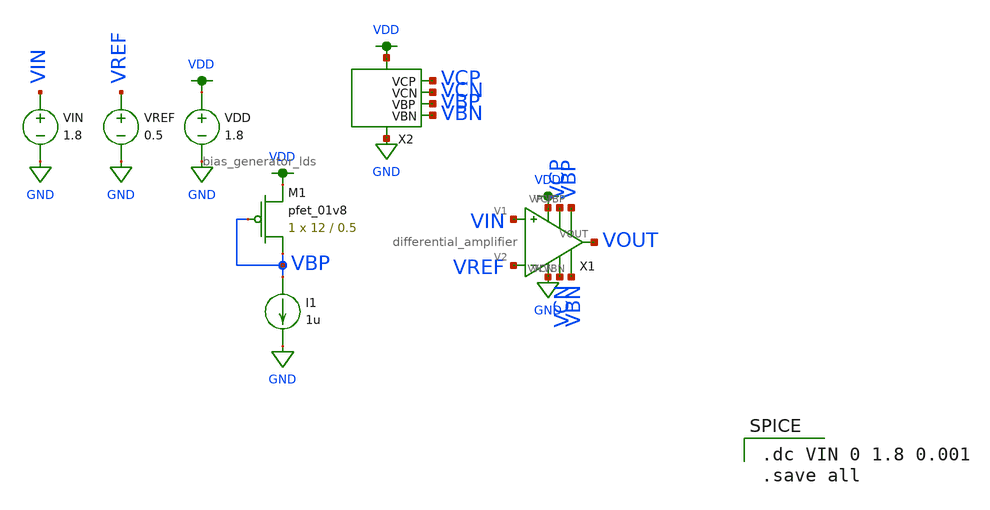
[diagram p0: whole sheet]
** sch_path: mp3/schematics/bias_generator_tran.sch
**.subckt bias_generator_tran
VDD VDD GND 1.8
I1 VBP GND 1u
VREF VREF GND 0.5
VIN VIN GND 1.8
XM1 VBP VBP VDD VDD sky130_fd_pr__pfet_01v8 L=0.5 W=12 nf=1 ad='int((nf+1)/2) * W/nf * 0.29' as='int((nf+2)/2) * W/nf * 0.29'
+ pd='2*int((nf+1)/2) * (W/nf + 0.29)' ps='2*int((nf+2)/2) * (W/nf + 0.29)' nrd='0.29 / W' nrs='0.29 / W'
+ sa=0 sb=0 sd=0 mult=1 m=1
X1 VIN VREF VDD GND VCN VBN VBP VCP VOUT differential_amplifier
X2 VDD GND VCN VCP VBP VBN bias_generator_lds
**** begin user architecture code

.option wnflag=1
.lib ~/skywater/skywater-pdk/libraries/sky130_fd_pr_ngspice/latest/models/sky130.lib.spice tt


.dc VIN 0 1.8 0.001
.save all

**** end user architecture code
**.ends

* expanding   symbol:  /home/madvlsi/Documents/VLSI/mp3/schematics/differential_amplifier.sym # of
*+ pins=9
** sym_path: mp3/schematics/differential_amplifier.sym
** sch_path: mp3/schematics/differential_amplifier.sch
.subckt differential_amplifier V1 V2 VP VN VCN VBN VBP VCP VOUT
*.iopin VBP
*.iopin VCP
*.ipin V1
*.ipin V2
*.iopin VBN
*.iopin VCN
*.iopin VP
*.iopin VN
*.opin VOUT
XM3b VP VBP net1 VDD sky130_fd_pr__pfet_01v8 L=0.5 W=3 nf=1 ad='int((nf+1)/2) * W/nf * 0.29' as='int((nf+2)/2) * W/nf * 0.29'
+ pd='2*int((nf+1)/2) * (W/nf + 0.29)' ps='2*int((nf+2)/2) * (W/nf + 0.29)' nrd='0.29 / W' nrs='0.29 / W'
+ sa=0 sb=0 sd=0 mult=1 m=1
XM3a net2 VBP VP VDD sky130_fd_pr__pfet_01v8 L=0.5 W=3 nf=1 ad='int((nf+1)/2) * W/nf * 0.29' as='int((nf+2)/2) * W/nf * 0.29'
+ pd='2*int((nf+1)/2) * (W/nf + 0.29)' ps='2*int((nf+2)/2) * (W/nf + 0.29)' nrd='0.29 / W' nrs='0.29 / W'
+ sa=0 sb=0 sd=0 mult=1 m=1
XM4a net1 VBP VP VDD sky130_fd_pr__pfet_01v8 L=0.5 W=3 nf=1 ad='int((nf+1)/2) * W/nf * 0.29' as='int((nf+2)/2) * W/nf * 0.29'
+ pd='2*int((nf+1)/2) * (W/nf + 0.29)' ps='2*int((nf+2)/2) * (W/nf + 0.29)' nrd='0.29 / W' nrs='0.29 / W'
+ sa=0 sb=0 sd=0 mult=1 m=1
XM4b VP VBP net2 VDD sky130_fd_pr__pfet_01v8 L=0.5 W=3 nf=1 ad='int((nf+1)/2) * W/nf * 0.29' as='int((nf+2)/2) * W/nf * 0.29'
+ pd='2*int((nf+1)/2) * (W/nf + 0.29)' ps='2*int((nf+2)/2) * (W/nf + 0.29)' nrd='0.29 / W' nrs='0.29 / W'
+ sa=0 sb=0 sd=0 mult=1 m=1
XM3c net2 VBP VP VDD sky130_fd_pr__pfet_01v8 L=0.5 W=3 nf=1 ad='int((nf+1)/2) * W/nf * 0.29' as='int((nf+2)/2) * W/nf * 0.29'
+ pd='2*int((nf+1)/2) * (W/nf + 0.29)' ps='2*int((nf+2)/2) * (W/nf + 0.29)' nrd='0.29 / W' nrs='0.29 / W'
+ sa=0 sb=0 sd=0 mult=1 m=1
XM3d VP VBP net1 VDD sky130_fd_pr__pfet_01v8 L=0.5 W=3 nf=1 ad='int((nf+1)/2) * W/nf * 0.29' as='int((nf+2)/2) * W/nf * 0.29'
+ pd='2*int((nf+1)/2) * (W/nf + 0.29)' ps='2*int((nf+2)/2) * (W/nf + 0.29)' nrd='0.29 / W' nrs='0.29 / W'
+ sa=0 sb=0 sd=0 mult=1 m=1
XM4c net1 VBP VP VDD sky130_fd_pr__pfet_01v8 L=0.5 W=3 nf=1 ad='int((nf+1)/2) * W/nf * 0.29' as='int((nf+2)/2) * W/nf * 0.29'
+ pd='2*int((nf+1)/2) * (W/nf + 0.29)' ps='2*int((nf+2)/2) * (W/nf + 0.29)' nrd='0.29 / W' nrs='0.29 / W'
+ sa=0 sb=0 sd=0 mult=1 m=1
XM1e VP VP net2 VP sky130_fd_pr__pfet_01v8 L=0.5 W=3 nf=1 ad='int((nf+1)/2) * W/nf * 0.29' as='int((nf+2)/2) * W/nf * 0.29'
+ pd='2*int((nf+1)/2) * (W/nf + 0.29)' ps='2*int((nf+2)/2) * (W/nf + 0.29)' nrd='0.29 / W' nrs='0.29 / W'
+ sa=0 sb=0 sd=0 mult=1 m=1
XM1f net2 VP VP VP sky130_fd_pr__pfet_01v8 L=0.5 W=3 nf=1 ad='int((nf+1)/2) * W/nf * 0.29' as='int((nf+2)/2) * W/nf * 0.29'
+ pd='2*int((nf+1)/2) * (W/nf + 0.29)' ps='2*int((nf+2)/2) * (W/nf + 0.29)' nrd='0.29 / W' nrs='0.29 / W'
+ sa=0 sb=0 sd=0 mult=1 m=1
XM4d VP VBP net2 VDD sky130_fd_pr__pfet_01v8 L=0.5 W=3 nf=1 ad='int((nf+1)/2) * W/nf * 0.29' as='int((nf+2)/2) * W/nf * 0.29'
+ pd='2*int((nf+1)/2) * (W/nf + 0.29)' ps='2*int((nf+2)/2) * (W/nf + 0.29)' nrd='0.29 / W' nrs='0.29 / W'
+ sa=0 sb=0 sd=0 mult=1 m=1
XM1 net2 VCP VOUT VDD sky130_fd_pr__pfet_01v8 L=0.5 W=3 nf=1 ad='int((nf+1)/2) * W/nf * 0.29' as='int((nf+2)/2) * W/nf * 0.29'
+ pd='2*int((nf+1)/2) * (W/nf + 0.29)' ps='2*int((nf+2)/2) * (W/nf + 0.29)' nrd='0.29 / W' nrs='0.29 / W'
+ sa=0 sb=0 sd=0 mult=1 m=1
XM2 VOUT VCP net2 VDD sky130_fd_pr__pfet_01v8 L=0.5 W=3 nf=1 ad='int((nf+1)/2) * W/nf * 0.29' as='int((nf+2)/2) * W/nf * 0.29'
+ pd='2*int((nf+1)/2) * (W/nf + 0.29)' ps='2*int((nf+2)/2) * (W/nf + 0.29)' nrd='0.29 / W' nrs='0.29 / W'
+ sa=0 sb=0 sd=0 mult=1 m=1
XM3 net3 VCP net1 VDD sky130_fd_pr__pfet_01v8 L=0.5 W=3 nf=1 ad='int((nf+1)/2) * W/nf * 0.29' as='int((nf+2)/2) * W/nf * 0.29'
+ pd='2*int((nf+1)/2) * (W/nf + 0.29)' ps='2*int((nf+2)/2) * (W/nf + 0.29)' nrd='0.29 / W' nrs='0.29 / W'
+ sa=0 sb=0 sd=0 mult=1 m=1
XM4 net1 VCP net3 VDD sky130_fd_pr__pfet_01v8 L=0.5 W=3 nf=1 ad='int((nf+1)/2) * W/nf * 0.29' as='int((nf+2)/2) * W/nf * 0.29'
+ pd='2*int((nf+1)/2) * (W/nf + 0.29)' ps='2*int((nf+2)/2) * (W/nf + 0.29)' nrd='0.29 / W' nrs='0.29 / W'
+ sa=0 sb=0 sd=0 mult=1 m=1
XM5 net3 VCP net1 VDD sky130_fd_pr__pfet_01v8 L=0.5 W=3 nf=1 ad='int((nf+1)/2) * W/nf * 0.29' as='int((nf+2)/2) * W/nf * 0.29'
+ pd='2*int((nf+1)/2) * (W/nf + 0.29)' ps='2*int((nf+2)/2) * (W/nf + 0.29)' nrd='0.29 / W' nrs='0.29 / W'
+ sa=0 sb=0 sd=0 mult=1 m=1
XM6 net1 VCP net3 VDD sky130_fd_pr__pfet_01v8 L=0.5 W=3 nf=1 ad='int((nf+1)/2) * W/nf * 0.29' as='int((nf+2)/2) * W/nf * 0.29'
+ pd='2*int((nf+1)/2) * (W/nf + 0.29)' ps='2*int((nf+2)/2) * (W/nf + 0.29)' nrd='0.29 / W' nrs='0.29 / W'
+ sa=0 sb=0 sd=0 mult=1 m=1
XM7 VOUT VCP net2 VDD sky130_fd_pr__pfet_01v8 L=0.5 W=3 nf=1 ad='int((nf+1)/2) * W/nf * 0.29' as='int((nf+2)/2) * W/nf * 0.29'
+ pd='2*int((nf+1)/2) * (W/nf + 0.29)' ps='2*int((nf+2)/2) * (W/nf + 0.29)' nrd='0.29 / W' nrs='0.29 / W'
+ sa=0 sb=0 sd=0 mult=1 m=1
XM8 VP VP VOUT VP sky130_fd_pr__pfet_01v8 L=0.5 W=3 nf=1 ad='int((nf+1)/2) * W/nf * 0.29' as='int((nf+2)/2) * W/nf * 0.29'
+ pd='2*int((nf+1)/2) * (W/nf + 0.29)' ps='2*int((nf+2)/2) * (W/nf + 0.29)' nrd='0.29 / W' nrs='0.29 / W'
+ sa=0 sb=0 sd=0 mult=1 m=1
XM9 VOUT VP VP VP sky130_fd_pr__pfet_01v8 L=0.5 W=3 nf=1 ad='int((nf+1)/2) * W/nf * 0.29' as='int((nf+2)/2) * W/nf * 0.29'
+ pd='2*int((nf+1)/2) * (W/nf + 0.29)' ps='2*int((nf+2)/2) * (W/nf + 0.29)' nrd='0.29 / W' nrs='0.29 / W'
+ sa=0 sb=0 sd=0 mult=1 m=1
XM10 net2 VCP VOUT VDD sky130_fd_pr__pfet_01v8 L=0.5 W=3 nf=1 ad='int((nf+1)/2) * W/nf * 0.29' as='int((nf+2)/2) * W/nf * 0.29'
+ pd='2*int((nf+1)/2) * (W/nf + 0.29)' ps='2*int((nf+2)/2) * (W/nf + 0.29)' nrd='0.29 / W' nrs='0.29 / W'
+ sa=0 sb=0 sd=0 mult=1 m=1
XM14 net4 V1 net1 GND sky130_fd_pr__nfet_01v8 L=0.5 W=3 nf=1 ad='int((nf+1)/2) * W/nf * 0.29' as='int((nf+2)/2) * W/nf * 0.29'
+ pd='2*int((nf+1)/2) * (W/nf + 0.29)' ps='2*int((nf+2)/2) * (W/nf + 0.29)' nrd='0.29 / W' nrs='0.29 / W'
+ sa=0 sb=0 sd=0 mult=1 m=1
XM22 net1 VN VN VN sky130_fd_pr__nfet_01v8 L=0.5 W=3 nf=1 ad='int((nf+1)/2) * W/nf * 0.29' as='int((nf+2)/2) * W/nf * 0.29'
+ pd='2*int((nf+1)/2) * (W/nf + 0.29)' ps='2*int((nf+2)/2) * (W/nf + 0.29)' nrd='0.29 / W' nrs='0.29 / W'
+ sa=0 sb=0 sd=0 mult=1 m=1
XM23 VN VN net1 VN sky130_fd_pr__nfet_01v8 L=0.5 W=3 nf=1 ad='int((nf+1)/2) * W/nf * 0.29' as='int((nf+2)/2) * W/nf * 0.29'
+ pd='2*int((nf+1)/2) * (W/nf + 0.29)' ps='2*int((nf+2)/2) * (W/nf + 0.29)' nrd='0.29 / W' nrs='0.29 / W'
+ sa=0 sb=0 sd=0 mult=1 m=1
XM15 net2 V2 net4 GND sky130_fd_pr__nfet_01v8 L=0.5 W=3 nf=1 ad='int((nf+1)/2) * W/nf * 0.29' as='int((nf+2)/2) * W/nf * 0.29'
+ pd='2*int((nf+1)/2) * (W/nf + 0.29)' ps='2*int((nf+2)/2) * (W/nf + 0.29)' nrd='0.29 / W' nrs='0.29 / W'
+ sa=0 sb=0 sd=0 mult=1 m=1
XM16 net4 V2 net2 GND sky130_fd_pr__nfet_01v8 L=0.5 W=3 nf=1 ad='int((nf+1)/2) * W/nf * 0.29' as='int((nf+2)/2) * W/nf * 0.29'
+ pd='2*int((nf+1)/2) * (W/nf + 0.29)' ps='2*int((nf+2)/2) * (W/nf + 0.29)' nrd='0.29 / W' nrs='0.29 / W'
+ sa=0 sb=0 sd=0 mult=1 m=1
XM17 net2 V2 net4 GND sky130_fd_pr__nfet_01v8 L=0.5 W=3 nf=1 ad='int((nf+1)/2) * W/nf * 0.29' as='int((nf+2)/2) * W/nf * 0.29'
+ pd='2*int((nf+1)/2) * (W/nf + 0.29)' ps='2*int((nf+2)/2) * (W/nf + 0.29)' nrd='0.29 / W' nrs='0.29 / W'
+ sa=0 sb=0 sd=0 mult=1 m=1
XM18 net1 V1 net4 GND sky130_fd_pr__nfet_01v8 L=0.5 W=3 nf=1 ad='int((nf+1)/2) * W/nf * 0.29' as='int((nf+2)/2) * W/nf * 0.29'
+ pd='2*int((nf+1)/2) * (W/nf + 0.29)' ps='2*int((nf+2)/2) * (W/nf + 0.29)' nrd='0.29 / W' nrs='0.29 / W'
+ sa=0 sb=0 sd=0 mult=1 m=1
XM19 net4 V1 net1 GND sky130_fd_pr__nfet_01v8 L=0.5 W=3 nf=1 ad='int((nf+1)/2) * W/nf * 0.29' as='int((nf+2)/2) * W/nf * 0.29'
+ pd='2*int((nf+1)/2) * (W/nf + 0.29)' ps='2*int((nf+2)/2) * (W/nf + 0.29)' nrd='0.29 / W' nrs='0.29 / W'
+ sa=0 sb=0 sd=0 mult=1 m=1
XM20 net4 V2 net2 GND sky130_fd_pr__nfet_01v8 L=0.5 W=3 nf=1 ad='int((nf+1)/2) * W/nf * 0.29' as='int((nf+2)/2) * W/nf * 0.29'
+ pd='2*int((nf+1)/2) * (W/nf + 0.29)' ps='2*int((nf+2)/2) * (W/nf + 0.29)' nrd='0.29 / W' nrs='0.29 / W'
+ sa=0 sb=0 sd=0 mult=1 m=1
XM21 net1 V1 net4 GND sky130_fd_pr__nfet_01v8 L=0.5 W=3 nf=1 ad='int((nf+1)/2) * W/nf * 0.29' as='int((nf+2)/2) * W/nf * 0.29'
+ pd='2*int((nf+1)/2) * (W/nf + 0.29)' ps='2*int((nf+2)/2) * (W/nf + 0.29)' nrd='0.29 / W' nrs='0.29 / W'
+ sa=0 sb=0 sd=0 mult=1 m=1
XM24 net4 VBN VN GND sky130_fd_pr__nfet_01v8 L=0.5 W=12 nf=1 ad='int((nf+1)/2) * W/nf * 0.29' as='int((nf+2)/2) * W/nf * 0.29'
+ pd='2*int((nf+1)/2) * (W/nf + 0.29)' ps='2*int((nf+2)/2) * (W/nf + 0.29)' nrd='0.29 / W' nrs='0.29 / W'
+ sa=0 sb=0 sd=0 mult=1 m=1
XM29 net3 VCN net6 GND sky130_fd_pr__nfet_01v8 L=0.5 W=3 nf=1 ad='int((nf+1)/2) * W/nf * 0.29' as='int((nf+2)/2) * W/nf * 0.29'
+ pd='2*int((nf+1)/2) * (W/nf + 0.29)' ps='2*int((nf+2)/2) * (W/nf + 0.29)' nrd='0.29 / W' nrs='0.29 / W'
+ sa=0 sb=0 sd=0 mult=1 m=1
XM30 net6 VCN net3 GND sky130_fd_pr__nfet_01v8 L=0.5 W=3 nf=1 ad='int((nf+1)/2) * W/nf * 0.29' as='int((nf+2)/2) * W/nf * 0.29'
+ pd='2*int((nf+1)/2) * (W/nf + 0.29)' ps='2*int((nf+2)/2) * (W/nf + 0.29)' nrd='0.29 / W' nrs='0.29 / W'
+ sa=0 sb=0 sd=0 mult=1 m=1
XM31 VOUT VCN net5 GND sky130_fd_pr__nfet_01v8 L=0.5 W=3 nf=1 ad='int((nf+1)/2) * W/nf * 0.29' as='int((nf+2)/2) * W/nf * 0.29'
+ pd='2*int((nf+1)/2) * (W/nf + 0.29)' ps='2*int((nf+2)/2) * (W/nf + 0.29)' nrd='0.29 / W' nrs='0.29 / W'
+ sa=0 sb=0 sd=0 mult=1 m=1
XM32 net5 VCN VOUT GND sky130_fd_pr__nfet_01v8 L=0.5 W=3 nf=1 ad='int((nf+1)/2) * W/nf * 0.29' as='int((nf+2)/2) * W/nf * 0.29'
+ pd='2*int((nf+1)/2) * (W/nf + 0.29)' ps='2*int((nf+2)/2) * (W/nf + 0.29)' nrd='0.29 / W' nrs='0.29 / W'
+ sa=0 sb=0 sd=0 mult=1 m=1
XM25 VOUT VCN net5 GND sky130_fd_pr__nfet_01v8 L=0.5 W=3 nf=1 ad='int((nf+1)/2) * W/nf * 0.29' as='int((nf+2)/2) * W/nf * 0.29'
+ pd='2*int((nf+1)/2) * (W/nf + 0.29)' ps='2*int((nf+2)/2) * (W/nf + 0.29)' nrd='0.29 / W' nrs='0.29 / W'
+ sa=0 sb=0 sd=0 mult=1 m=1
XM26 net5 VCN VOUT GND sky130_fd_pr__nfet_01v8 L=0.5 W=3 nf=1 ad='int((nf+1)/2) * W/nf * 0.29' as='int((nf+2)/2) * W/nf * 0.29'
+ pd='2*int((nf+1)/2) * (W/nf + 0.29)' ps='2*int((nf+2)/2) * (W/nf + 0.29)' nrd='0.29 / W' nrs='0.29 / W'
+ sa=0 sb=0 sd=0 mult=1 m=1
XM27 net3 VCN net6 GND sky130_fd_pr__nfet_01v8 L=0.5 W=3 nf=1 ad='int((nf+1)/2) * W/nf * 0.29' as='int((nf+2)/2) * W/nf * 0.29'
+ pd='2*int((nf+1)/2) * (W/nf + 0.29)' ps='2*int((nf+2)/2) * (W/nf + 0.29)' nrd='0.29 / W' nrs='0.29 / W'
+ sa=0 sb=0 sd=0 mult=1 m=1
XM28 net6 VCN net3 GND sky130_fd_pr__nfet_01v8 L=0.5 W=3 nf=1 ad='int((nf+1)/2) * W/nf * 0.29' as='int((nf+2)/2) * W/nf * 0.29'
+ pd='2*int((nf+1)/2) * (W/nf + 0.29)' ps='2*int((nf+2)/2) * (W/nf + 0.29)' nrd='0.29 / W' nrs='0.29 / W'
+ sa=0 sb=0 sd=0 mult=1 m=1
XM35 net6 net3 VN GND sky130_fd_pr__nfet_01v8 L=0.5 W=3 nf=1 ad='int((nf+1)/2) * W/nf * 0.29' as='int((nf+2)/2) * W/nf * 0.29'
+ pd='2*int((nf+1)/2) * (W/nf + 0.29)' ps='2*int((nf+2)/2) * (W/nf + 0.29)' nrd='0.29 / W' nrs='0.29 / W'
+ sa=0 sb=0 sd=0 mult=1 m=1
XM36 VN net3 net6 GND sky130_fd_pr__nfet_01v8 L=0.5 W=3 nf=1 ad='int((nf+1)/2) * W/nf * 0.29' as='int((nf+2)/2) * W/nf * 0.29'
+ pd='2*int((nf+1)/2) * (W/nf + 0.29)' ps='2*int((nf+2)/2) * (W/nf + 0.29)' nrd='0.29 / W' nrs='0.29 / W'
+ sa=0 sb=0 sd=0 mult=1 m=1
XM37 net5 net3 VN GND sky130_fd_pr__nfet_01v8 L=0.5 W=3 nf=1 ad='int((nf+1)/2) * W/nf * 0.29' as='int((nf+2)/2) * W/nf * 0.29'
+ pd='2*int((nf+1)/2) * (W/nf + 0.29)' ps='2*int((nf+2)/2) * (W/nf + 0.29)' nrd='0.29 / W' nrs='0.29 / W'
+ sa=0 sb=0 sd=0 mult=1 m=1
XM38 VN net3 net5 GND sky130_fd_pr__nfet_01v8 L=0.5 W=3 nf=1 ad='int((nf+1)/2) * W/nf * 0.29' as='int((nf+2)/2) * W/nf * 0.29'
+ pd='2*int((nf+1)/2) * (W/nf + 0.29)' ps='2*int((nf+2)/2) * (W/nf + 0.29)' nrd='0.29 / W' nrs='0.29 / W'
+ sa=0 sb=0 sd=0 mult=1 m=1
XM39 net5 net3 VN GND sky130_fd_pr__nfet_01v8 L=0.5 W=3 nf=1 ad='int((nf+1)/2) * W/nf * 0.29' as='int((nf+2)/2) * W/nf * 0.29'
+ pd='2*int((nf+1)/2) * (W/nf + 0.29)' ps='2*int((nf+2)/2) * (W/nf + 0.29)' nrd='0.29 / W' nrs='0.29 / W'
+ sa=0 sb=0 sd=0 mult=1 m=1
XM40 VN net3 net5 GND sky130_fd_pr__nfet_01v8 L=0.5 W=3 nf=1 ad='int((nf+1)/2) * W/nf * 0.29' as='int((nf+2)/2) * W/nf * 0.29'
+ pd='2*int((nf+1)/2) * (W/nf + 0.29)' ps='2*int((nf+2)/2) * (W/nf + 0.29)' nrd='0.29 / W' nrs='0.29 / W'
+ sa=0 sb=0 sd=0 mult=1 m=1
XM41 net6 net3 VN GND sky130_fd_pr__nfet_01v8 L=0.5 W=3 nf=1 ad='int((nf+1)/2) * W/nf * 0.29' as='int((nf+2)/2) * W/nf * 0.29'
+ pd='2*int((nf+1)/2) * (W/nf + 0.29)' ps='2*int((nf+2)/2) * (W/nf + 0.29)' nrd='0.29 / W' nrs='0.29 / W'
+ sa=0 sb=0 sd=0 mult=1 m=1
XM42 VN net3 net6 GND sky130_fd_pr__nfet_01v8 L=0.5 W=3 nf=1 ad='int((nf+1)/2) * W/nf * 0.29' as='int((nf+2)/2) * W/nf * 0.29'
+ pd='2*int((nf+1)/2) * (W/nf + 0.29)' ps='2*int((nf+2)/2) * (W/nf + 0.29)' nrd='0.29 / W' nrs='0.29 / W'
+ sa=0 sb=0 sd=0 mult=1 m=1
XM33 net5 VN VN VN sky130_fd_pr__nfet_01v8 L=0.5 W=3 nf=1 ad='int((nf+1)/2) * W/nf * 0.29' as='int((nf+2)/2) * W/nf * 0.29'
+ pd='2*int((nf+1)/2) * (W/nf + 0.29)' ps='2*int((nf+2)/2) * (W/nf + 0.29)' nrd='0.29 / W' nrs='0.29 / W'
+ sa=0 sb=0 sd=0 mult=1 m=1
XM34 VN VN VN VN sky130_fd_pr__nfet_01v8 L=0.5 W=3 nf=1 ad='int((nf+1)/2) * W/nf * 0.29' as='int((nf+2)/2) * W/nf * 0.29'
+ pd='2*int((nf+1)/2) * (W/nf + 0.29)' ps='2*int((nf+2)/2) * (W/nf + 0.29)' nrd='0.29 / W' nrs='0.29 / W'
+ sa=0 sb=0 sd=0 mult=1 m=1
XM43 VN VN net5 VN sky130_fd_pr__nfet_01v8 L=0.5 W=3 nf=1 ad='int((nf+1)/2) * W/nf * 0.29' as='int((nf+2)/2) * W/nf * 0.29'
+ pd='2*int((nf+1)/2) * (W/nf + 0.29)' ps='2*int((nf+2)/2) * (W/nf + 0.29)' nrd='0.29 / W' nrs='0.29 / W'
+ sa=0 sb=0 sd=0 mult=1 m=1
XM44 VN VN VN VN sky130_fd_pr__nfet_01v8 L=0.5 W=3 nf=1 ad='int((nf+1)/2) * W/nf * 0.29' as='int((nf+2)/2) * W/nf * 0.29'
+ pd='2*int((nf+1)/2) * (W/nf + 0.29)' ps='2*int((nf+2)/2) * (W/nf + 0.29)' nrd='0.29 / W' nrs='0.29 / W'
+ sa=0 sb=0 sd=0 mult=1 m=1
.ends


* expanding   symbol:  /home/madvlsi/Documents/VLSI/mp3/schematics/bias_generator_lds.sym # of
*+ pins=6
** sym_path: mp3/schematics/bias_generator_lds.sym
** sch_path: mp3/schematics/bias_generator_lds.sch
.subckt bias_generator_lds VP VN VCN VCP VBP VBN
*.iopin VBP
*.iopin VP
*.iopin VN
*.opin VCN
*.opin VCP
*.opin VBN
XM9 VCN VP VP VP sky130_fd_pr__pfet_01v8 L=0.5 W=12 nf=1 ad='int((nf+1)/2) * W/nf * 0.29' as='int((nf+2)/2) * W/nf * 0.29'
+ pd='2*int((nf+1)/2) * (W/nf + 0.29)' ps='2*int((nf+2)/2) * (W/nf + 0.29)' nrd='0.29 / W' nrs='0.29 / W'
+ sa=0 sb=0 sd=0 mult=1 m=1
XM24 net11 VCN net10 GND sky130_fd_pr__nfet_01v8 L=0.5 W=12 nf=1 ad='int((nf+1)/2) * W/nf * 0.29' as='int((nf+2)/2) * W/nf * 0.29'
+ pd='2*int((nf+1)/2) * (W/nf + 0.29)' ps='2*int((nf+2)/2) * (W/nf + 0.29)' nrd='0.29 / W' nrs='0.29 / W'
+ sa=0 sb=0 sd=0 mult=1 m=1
XM2 VCN VBP VP VDD sky130_fd_pr__pfet_01v8 L=0.5 W=12 nf=1 ad='int((nf+1)/2) * W/nf * 0.29' as='int((nf+2)/2) * W/nf * 0.29'
+ pd='2*int((nf+1)/2) * (W/nf + 0.29)' ps='2*int((nf+2)/2) * (W/nf + 0.29)' nrd='0.29 / W' nrs='0.29 / W'
+ sa=0 sb=0 sd=0 mult=1 m=1
XM1 VP VBP net1 VDD sky130_fd_pr__pfet_01v8 L=0.5 W=12 nf=1 ad='int((nf+1)/2) * W/nf * 0.29' as='int((nf+2)/2) * W/nf * 0.29'
+ pd='2*int((nf+1)/2) * (W/nf + 0.29)' ps='2*int((nf+2)/2) * (W/nf + 0.29)' nrd='0.29 / W' nrs='0.29 / W'
+ sa=0 sb=0 sd=0 mult=1 m=1
XM3 net1 VBP net2 VDD sky130_fd_pr__pfet_01v8 L=0.5 W=12 nf=1 ad='int((nf+1)/2) * W/nf * 0.29' as='int((nf+2)/2) * W/nf * 0.29'
+ pd='2*int((nf+1)/2) * (W/nf + 0.29)' ps='2*int((nf+2)/2) * (W/nf + 0.29)' nrd='0.29 / W' nrs='0.29 / W'
+ sa=0 sb=0 sd=0 mult=1 m=1
XM4 net2 VBP net3 VDD sky130_fd_pr__pfet_01v8 L=0.5 W=12 nf=1 ad='int((nf+1)/2) * W/nf * 0.29' as='int((nf+2)/2) * W/nf * 0.29'
+ pd='2*int((nf+1)/2) * (W/nf + 0.29)' ps='2*int((nf+2)/2) * (W/nf + 0.29)' nrd='0.29 / W' nrs='0.29 / W'
+ sa=0 sb=0 sd=0 mult=1 m=1
XM6 net3 VBP net4 VDD sky130_fd_pr__pfet_01v8 L=0.5 W=12 nf=1 ad='int((nf+1)/2) * W/nf * 0.29' as='int((nf+2)/2) * W/nf * 0.29'
+ pd='2*int((nf+1)/2) * (W/nf + 0.29)' ps='2*int((nf+2)/2) * (W/nf + 0.29)' nrd='0.29 / W' nrs='0.29 / W'
+ sa=0 sb=0 sd=0 mult=1 m=1
XM7 net4 VBP net9 VDD sky130_fd_pr__pfet_01v8 L=0.5 W=12 nf=1 ad='int((nf+1)/2) * W/nf * 0.29' as='int((nf+2)/2) * W/nf * 0.29'
+ pd='2*int((nf+1)/2) * (W/nf + 0.29)' ps='2*int((nf+2)/2) * (W/nf + 0.29)' nrd='0.29 / W' nrs='0.29 / W'
+ sa=0 sb=0 sd=0 mult=1 m=1
XM8 net9 VBP net5 VDD sky130_fd_pr__pfet_01v8 L=0.5 W=12 nf=1 ad='int((nf+1)/2) * W/nf * 0.29' as='int((nf+2)/2) * W/nf * 0.29'
+ pd='2*int((nf+1)/2) * (W/nf + 0.29)' ps='2*int((nf+2)/2) * (W/nf + 0.29)' nrd='0.29 / W' nrs='0.29 / W'
+ sa=0 sb=0 sd=0 mult=1 m=1
XM52 net5 VBP net6 VDD sky130_fd_pr__pfet_01v8 L=0.5 W=12 nf=1 ad='int((nf+1)/2) * W/nf * 0.29' as='int((nf+2)/2) * W/nf * 0.29'
+ pd='2*int((nf+1)/2) * (W/nf + 0.29)' ps='2*int((nf+2)/2) * (W/nf + 0.29)' nrd='0.29 / W' nrs='0.29 / W'
+ sa=0 sb=0 sd=0 mult=1 m=1
XM53 net6 VBP net7 VDD sky130_fd_pr__pfet_01v8 L=0.5 W=12 nf=1 ad='int((nf+1)/2) * W/nf * 0.29' as='int((nf+2)/2) * W/nf * 0.29'
+ pd='2*int((nf+1)/2) * (W/nf + 0.29)' ps='2*int((nf+2)/2) * (W/nf + 0.29)' nrd='0.29 / W' nrs='0.29 / W'
+ sa=0 sb=0 sd=0 mult=1 m=1
XM54 net7 VBP net8 VDD sky130_fd_pr__pfet_01v8 L=0.5 W=12 nf=1 ad='int((nf+1)/2) * W/nf * 0.29' as='int((nf+2)/2) * W/nf * 0.29'
+ pd='2*int((nf+1)/2) * (W/nf + 0.29)' ps='2*int((nf+2)/2) * (W/nf + 0.29)' nrd='0.29 / W' nrs='0.29 / W'
+ sa=0 sb=0 sd=0 mult=1 m=1
XM55 net8 VBP VP VDD sky130_fd_pr__pfet_01v8 L=0.5 W=12 nf=1 ad='int((nf+1)/2) * W/nf * 0.29' as='int((nf+2)/2) * W/nf * 0.29'
+ pd='2*int((nf+1)/2) * (W/nf + 0.29)' ps='2*int((nf+2)/2) * (W/nf + 0.29)' nrd='0.29 / W' nrs='0.29 / W'
+ sa=0 sb=0 sd=0 mult=1 m=1
XM56 VP VBP VCN VDD sky130_fd_pr__pfet_01v8 L=0.5 W=12 nf=1 ad='int((nf+1)/2) * W/nf * 0.29' as='int((nf+2)/2) * W/nf * 0.29'
+ pd='2*int((nf+1)/2) * (W/nf + 0.29)' ps='2*int((nf+2)/2) * (W/nf + 0.29)' nrd='0.29 / W' nrs='0.29 / W'
+ sa=0 sb=0 sd=0 mult=1 m=1
XM10 VP VP VCN VP sky130_fd_pr__pfet_01v8 L=0.5 W=12 nf=1 ad='int((nf+1)/2) * W/nf * 0.29' as='int((nf+2)/2) * W/nf * 0.29'
+ pd='2*int((nf+1)/2) * (W/nf + 0.29)' ps='2*int((nf+2)/2) * (W/nf + 0.29)' nrd='0.29 / W' nrs='0.29 / W'
+ sa=0 sb=0 sd=0 mult=1 m=1
XM25 VN VN net11 VN sky130_fd_pr__nfet_01v8 L=0.5 W=12 nf=1 ad='int((nf+1)/2) * W/nf * 0.29' as='int((nf+2)/2) * W/nf * 0.29'
+ pd='2*int((nf+1)/2) * (W/nf + 0.29)' ps='2*int((nf+2)/2) * (W/nf + 0.29)' nrd='0.29 / W' nrs='0.29 / W'
+ sa=0 sb=0 sd=0 mult=1 m=1
XM14 net9 net9 net10 GND sky130_fd_pr__nfet_01v8 L=0.5 W=12 nf=1 ad='int((nf+1)/2) * W/nf * 0.29' as='int((nf+2)/2) * W/nf * 0.29'
+ pd='2*int((nf+1)/2) * (W/nf + 0.29)' ps='2*int((nf+2)/2) * (W/nf + 0.29)' nrd='0.29 / W' nrs='0.29 / W'
+ sa=0 sb=0 sd=0 mult=1 m=1
XM15 net10 net9 net9 GND sky130_fd_pr__nfet_01v8 L=0.5 W=12 nf=1 ad='int((nf+1)/2) * W/nf * 0.29' as='int((nf+2)/2) * W/nf * 0.29'
+ pd='2*int((nf+1)/2) * (W/nf + 0.29)' ps='2*int((nf+2)/2) * (W/nf + 0.29)' nrd='0.29 / W' nrs='0.29 / W'
+ sa=0 sb=0 sd=0 mult=1 m=1
XM16 net9 net9 net10 GND sky130_fd_pr__nfet_01v8 L=0.5 W=12 nf=1 ad='int((nf+1)/2) * W/nf * 0.29' as='int((nf+2)/2) * W/nf * 0.29'
+ pd='2*int((nf+1)/2) * (W/nf + 0.29)' ps='2*int((nf+2)/2) * (W/nf + 0.29)' nrd='0.29 / W' nrs='0.29 / W'
+ sa=0 sb=0 sd=0 mult=1 m=1
XM17 net10 net9 net9 GND sky130_fd_pr__nfet_01v8 L=0.5 W=12 nf=1 ad='int((nf+1)/2) * W/nf * 0.29' as='int((nf+2)/2) * W/nf * 0.29'
+ pd='2*int((nf+1)/2) * (W/nf + 0.29)' ps='2*int((nf+2)/2) * (W/nf + 0.29)' nrd='0.29 / W' nrs='0.29 / W'
+ sa=0 sb=0 sd=0 mult=1 m=1
XM18 VN net9 net10 GND sky130_fd_pr__nfet_01v8 L=0.5 W=12 nf=1 ad='int((nf+1)/2) * W/nf * 0.29' as='int((nf+2)/2) * W/nf * 0.29'
+ pd='2*int((nf+1)/2) * (W/nf + 0.29)' ps='2*int((nf+2)/2) * (W/nf + 0.29)' nrd='0.29 / W' nrs='0.29 / W'
+ sa=0 sb=0 sd=0 mult=1 m=1
XM19 net10 net9 VN GND sky130_fd_pr__nfet_01v8 L=0.5 W=12 nf=1 ad='int((nf+1)/2) * W/nf * 0.29' as='int((nf+2)/2) * W/nf * 0.29'
+ pd='2*int((nf+1)/2) * (W/nf + 0.29)' ps='2*int((nf+2)/2) * (W/nf + 0.29)' nrd='0.29 / W' nrs='0.29 / W'
+ sa=0 sb=0 sd=0 mult=1 m=1
XM20 net9 net9 net10 GND sky130_fd_pr__nfet_01v8 L=0.5 W=12 nf=1 ad='int((nf+1)/2) * W/nf * 0.29' as='int((nf+2)/2) * W/nf * 0.29'
+ pd='2*int((nf+1)/2) * (W/nf + 0.29)' ps='2*int((nf+2)/2) * (W/nf + 0.29)' nrd='0.29 / W' nrs='0.29 / W'
+ sa=0 sb=0 sd=0 mult=1 m=1
XM21 net10 net9 net9 GND sky130_fd_pr__nfet_01v8 L=0.5 W=12 nf=1 ad='int((nf+1)/2) * W/nf * 0.29' as='int((nf+2)/2) * W/nf * 0.29'
+ pd='2*int((nf+1)/2) * (W/nf + 0.29)' ps='2*int((nf+2)/2) * (W/nf + 0.29)' nrd='0.29 / W' nrs='0.29 / W'
+ sa=0 sb=0 sd=0 mult=1 m=1
XM22 net9 net9 net10 GND sky130_fd_pr__nfet_01v8 L=0.5 W=12 nf=1 ad='int((nf+1)/2) * W/nf * 0.29' as='int((nf+2)/2) * W/nf * 0.29'
+ pd='2*int((nf+1)/2) * (W/nf + 0.29)' ps='2*int((nf+2)/2) * (W/nf + 0.29)' nrd='0.29 / W' nrs='0.29 / W'
+ sa=0 sb=0 sd=0 mult=1 m=1
XM23 net10 net9 net9 GND sky130_fd_pr__nfet_01v8 L=0.5 W=12 nf=1 ad='int((nf+1)/2) * W/nf * 0.29' as='int((nf+2)/2) * W/nf * 0.29'
+ pd='2*int((nf+1)/2) * (W/nf + 0.29)' ps='2*int((nf+2)/2) * (W/nf + 0.29)' nrd='0.29 / W' nrs='0.29 / W'
+ sa=0 sb=0 sd=0 mult=1 m=1
XM5 net10 VCN VCN GND sky130_fd_pr__nfet_01v8 L=0.5 W=12 nf=1 ad='int((nf+1)/2) * W/nf * 0.29' as='int((nf+2)/2) * W/nf * 0.29'
+ pd='2*int((nf+1)/2) * (W/nf + 0.29)' ps='2*int((nf+2)/2) * (W/nf + 0.29)' nrd='0.29 / W' nrs='0.29 / W'
+ sa=0 sb=0 sd=0 mult=1 m=1
XM26 VCN VN VN VN sky130_fd_pr__nfet_01v8 L=0.5 W=12 nf=1 ad='int((nf+1)/2) * W/nf * 0.29' as='int((nf+2)/2) * W/nf * 0.29'
+ pd='2*int((nf+1)/2) * (W/nf + 0.29)' ps='2*int((nf+2)/2) * (W/nf + 0.29)' nrd='0.29 / W' nrs='0.29 / W'
+ sa=0 sb=0 sd=0 mult=1 m=1
XM27 net14 VBN VN GND sky130_fd_pr__nfet_01v8 L=0.5 W=12 nf=1 ad='int((nf+1)/2) * W/nf * 0.29' as='int((nf+2)/2) * W/nf * 0.29'
+ pd='2*int((nf+1)/2) * (W/nf + 0.29)' ps='2*int((nf+2)/2) * (W/nf + 0.29)' nrd='0.29 / W' nrs='0.29 / W'
+ sa=0 sb=0 sd=0 mult=1 m=1
XM39 net15 VBN net14 GND sky130_fd_pr__nfet_01v8 L=0.5 W=12 nf=1 ad='int((nf+1)/2) * W/nf * 0.29' as='int((nf+2)/2) * W/nf * 0.29'
+ pd='2*int((nf+1)/2) * (W/nf + 0.29)' ps='2*int((nf+2)/2) * (W/nf + 0.29)' nrd='0.29 / W' nrs='0.29 / W'
+ sa=0 sb=0 sd=0 mult=1 m=1
XM40 net16 VBN net15 GND sky130_fd_pr__nfet_01v8 L=0.5 W=12 nf=1 ad='int((nf+1)/2) * W/nf * 0.29' as='int((nf+2)/2) * W/nf * 0.29'
+ pd='2*int((nf+1)/2) * (W/nf + 0.29)' ps='2*int((nf+2)/2) * (W/nf + 0.29)' nrd='0.29 / W' nrs='0.29 / W'
+ sa=0 sb=0 sd=0 mult=1 m=1
XM41 net17 VBN net16 GND sky130_fd_pr__nfet_01v8 L=0.5 W=12 nf=1 ad='int((nf+1)/2) * W/nf * 0.29' as='int((nf+2)/2) * W/nf * 0.29'
+ pd='2*int((nf+1)/2) * (W/nf + 0.29)' ps='2*int((nf+2)/2) * (W/nf + 0.29)' nrd='0.29 / W' nrs='0.29 / W'
+ sa=0 sb=0 sd=0 mult=1 m=1
XM42 net12 VBN net17 GND sky130_fd_pr__nfet_01v8 L=0.5 W=12 nf=1 ad='int((nf+1)/2) * W/nf * 0.29' as='int((nf+2)/2) * W/nf * 0.29'
+ pd='2*int((nf+1)/2) * (W/nf + 0.29)' ps='2*int((nf+2)/2) * (W/nf + 0.29)' nrd='0.29 / W' nrs='0.29 / W'
+ sa=0 sb=0 sd=0 mult=1 m=1
XM43 net18 VBN net12 GND sky130_fd_pr__nfet_01v8 L=0.5 W=12 nf=1 ad='int((nf+1)/2) * W/nf * 0.29' as='int((nf+2)/2) * W/nf * 0.29'
+ pd='2*int((nf+1)/2) * (W/nf + 0.29)' ps='2*int((nf+2)/2) * (W/nf + 0.29)' nrd='0.29 / W' nrs='0.29 / W'
+ sa=0 sb=0 sd=0 mult=1 m=1
XM44 net19 VBN net18 GND sky130_fd_pr__nfet_01v8 L=0.5 W=12 nf=1 ad='int((nf+1)/2) * W/nf * 0.29' as='int((nf+2)/2) * W/nf * 0.29'
+ pd='2*int((nf+1)/2) * (W/nf + 0.29)' ps='2*int((nf+2)/2) * (W/nf + 0.29)' nrd='0.29 / W' nrs='0.29 / W'
+ sa=0 sb=0 sd=0 mult=1 m=1
XM45 net20 VBN net19 GND sky130_fd_pr__nfet_01v8 L=0.5 W=12 nf=1 ad='int((nf+1)/2) * W/nf * 0.29' as='int((nf+2)/2) * W/nf * 0.29'
+ pd='2*int((nf+1)/2) * (W/nf + 0.29)' ps='2*int((nf+2)/2) * (W/nf + 0.29)' nrd='0.29 / W' nrs='0.29 / W'
+ sa=0 sb=0 sd=0 mult=1 m=1
XM46 net21 VBN net20 GND sky130_fd_pr__nfet_01v8 L=0.5 W=12 nf=1 ad='int((nf+1)/2) * W/nf * 0.29' as='int((nf+2)/2) * W/nf * 0.29'
+ pd='2*int((nf+1)/2) * (W/nf + 0.29)' ps='2*int((nf+2)/2) * (W/nf + 0.29)' nrd='0.29 / W' nrs='0.29 / W'
+ sa=0 sb=0 sd=0 mult=1 m=1
XM47 VN VBN net21 GND sky130_fd_pr__nfet_01v8 L=0.5 W=12 nf=1 ad='int((nf+1)/2) * W/nf * 0.29' as='int((nf+2)/2) * W/nf * 0.29'
+ pd='2*int((nf+1)/2) * (W/nf + 0.29)' ps='2*int((nf+2)/2) * (W/nf + 0.29)' nrd='0.29 / W' nrs='0.29 / W'
+ sa=0 sb=0 sd=0 mult=1 m=1
XM48 VN VBN VCP GND sky130_fd_pr__nfet_01v8 L=0.5 W=12 nf=1 ad='int((nf+1)/2) * W/nf * 0.29' as='int((nf+2)/2) * W/nf * 0.29'
+ pd='2*int((nf+1)/2) * (W/nf + 0.29)' ps='2*int((nf+2)/2) * (W/nf + 0.29)' nrd='0.29 / W' nrs='0.29 / W'
+ sa=0 sb=0 sd=0 mult=1 m=1
XM49 VCP VBN VN GND sky130_fd_pr__nfet_01v8 L=0.5 W=12 nf=1 ad='int((nf+1)/2) * W/nf * 0.29' as='int((nf+2)/2) * W/nf * 0.29'
+ pd='2*int((nf+1)/2) * (W/nf + 0.29)' ps='2*int((nf+2)/2) * (W/nf + 0.29)' nrd='0.29 / W' nrs='0.29 / W'
+ sa=0 sb=0 sd=0 mult=1 m=1
XM29 net13 net12 net12 VDD sky130_fd_pr__pfet_01v8 L=0.5 W=12 nf=1 ad='int((nf+1)/2) * W/nf * 0.29' as='int((nf+2)/2) * W/nf * 0.29'
+ pd='2*int((nf+1)/2) * (W/nf + 0.29)' ps='2*int((nf+2)/2) * (W/nf + 0.29)' nrd='0.29 / W' nrs='0.29 / W'
+ sa=0 sb=0 sd=0 mult=1 m=1
XM30 net12 net12 net13 VDD sky130_fd_pr__pfet_01v8 L=0.5 W=12 nf=1 ad='int((nf+1)/2) * W/nf * 0.29' as='int((nf+2)/2) * W/nf * 0.29'
+ pd='2*int((nf+1)/2) * (W/nf + 0.29)' ps='2*int((nf+2)/2) * (W/nf + 0.29)' nrd='0.29 / W' nrs='0.29 / W'
+ sa=0 sb=0 sd=0 mult=1 m=1
XM31 net13 net12 net12 VDD sky130_fd_pr__pfet_01v8 L=0.5 W=12 nf=1 ad='int((nf+1)/2) * W/nf * 0.29' as='int((nf+2)/2) * W/nf * 0.29'
+ pd='2*int((nf+1)/2) * (W/nf + 0.29)' ps='2*int((nf+2)/2) * (W/nf + 0.29)' nrd='0.29 / W' nrs='0.29 / W'
+ sa=0 sb=0 sd=0 mult=1 m=1
XM32 net12 net12 net13 VDD sky130_fd_pr__pfet_01v8 L=0.5 W=12 nf=1 ad='int((nf+1)/2) * W/nf * 0.29' as='int((nf+2)/2) * W/nf * 0.29'
+ pd='2*int((nf+1)/2) * (W/nf + 0.29)' ps='2*int((nf+2)/2) * (W/nf + 0.29)' nrd='0.29 / W' nrs='0.29 / W'
+ sa=0 sb=0 sd=0 mult=1 m=1
XM33 net13 net12 VP VDD sky130_fd_pr__pfet_01v8 L=0.5 W=12 nf=1 ad='int((nf+1)/2) * W/nf * 0.29' as='int((nf+2)/2) * W/nf * 0.29'
+ pd='2*int((nf+1)/2) * (W/nf + 0.29)' ps='2*int((nf+2)/2) * (W/nf + 0.29)' nrd='0.29 / W' nrs='0.29 / W'
+ sa=0 sb=0 sd=0 mult=1 m=1
XM34 VP net12 net13 VDD sky130_fd_pr__pfet_01v8 L=0.5 W=12 nf=1 ad='int((nf+1)/2) * W/nf * 0.29' as='int((nf+2)/2) * W/nf * 0.29'
+ pd='2*int((nf+1)/2) * (W/nf + 0.29)' ps='2*int((nf+2)/2) * (W/nf + 0.29)' nrd='0.29 / W' nrs='0.29 / W'
+ sa=0 sb=0 sd=0 mult=1 m=1
XM35 net13 net12 net12 VDD sky130_fd_pr__pfet_01v8 L=0.5 W=12 nf=1 ad='int((nf+1)/2) * W/nf * 0.29' as='int((nf+2)/2) * W/nf * 0.29'
+ pd='2*int((nf+1)/2) * (W/nf + 0.29)' ps='2*int((nf+2)/2) * (W/nf + 0.29)' nrd='0.29 / W' nrs='0.29 / W'
+ sa=0 sb=0 sd=0 mult=1 m=1
XM36 net12 net12 net13 VDD sky130_fd_pr__pfet_01v8 L=0.5 W=12 nf=1 ad='int((nf+1)/2) * W/nf * 0.29' as='int((nf+2)/2) * W/nf * 0.29'
+ pd='2*int((nf+1)/2) * (W/nf + 0.29)' ps='2*int((nf+2)/2) * (W/nf + 0.29)' nrd='0.29 / W' nrs='0.29 / W'
+ sa=0 sb=0 sd=0 mult=1 m=1
XM37 net13 net12 net12 VDD sky130_fd_pr__pfet_01v8 L=0.5 W=12 nf=1 ad='int((nf+1)/2) * W/nf * 0.29' as='int((nf+2)/2) * W/nf * 0.29'
+ pd='2*int((nf+1)/2) * (W/nf + 0.29)' ps='2*int((nf+2)/2) * (W/nf + 0.29)' nrd='0.29 / W' nrs='0.29 / W'
+ sa=0 sb=0 sd=0 mult=1 m=1
XM38 net12 net12 net13 VDD sky130_fd_pr__pfet_01v8 L=0.5 W=12 nf=1 ad='int((nf+1)/2) * W/nf * 0.29' as='int((nf+2)/2) * W/nf * 0.29'
+ pd='2*int((nf+1)/2) * (W/nf + 0.29)' ps='2*int((nf+2)/2) * (W/nf + 0.29)' nrd='0.29 / W' nrs='0.29 / W'
+ sa=0 sb=0 sd=0 mult=1 m=1
XM57 VCP VCP net13 VDD sky130_fd_pr__pfet_01v8 L=0.5 W=12 nf=1 ad='int((nf+1)/2) * W/nf * 0.29' as='int((nf+2)/2) * W/nf * 0.29'
+ pd='2*int((nf+1)/2) * (W/nf + 0.29)' ps='2*int((nf+2)/2) * (W/nf + 0.29)' nrd='0.29 / W' nrs='0.29 / W'
+ sa=0 sb=0 sd=0 mult=1 m=1
XM28 net13 VCP VCP VDD sky130_fd_pr__pfet_01v8 L=0.5 W=12 nf=1 ad='int((nf+1)/2) * W/nf * 0.29' as='int((nf+2)/2) * W/nf * 0.29'
+ pd='2*int((nf+1)/2) * (W/nf + 0.29)' ps='2*int((nf+2)/2) * (W/nf + 0.29)' nrd='0.29 / W' nrs='0.29 / W'
+ sa=0 sb=0 sd=0 mult=1 m=1
XM50 VCP VP VP VP sky130_fd_pr__pfet_01v8 L=0.5 W=12 nf=1 ad='int((nf+1)/2) * W/nf * 0.29' as='int((nf+2)/2) * W/nf * 0.29'
+ pd='2*int((nf+1)/2) * (W/nf + 0.29)' ps='2*int((nf+2)/2) * (W/nf + 0.29)' nrd='0.29 / W' nrs='0.29 / W'
+ sa=0 sb=0 sd=0 mult=1 m=1
XM51 VP VP VCP VP sky130_fd_pr__pfet_01v8 L=0.5 W=12 nf=1 ad='int((nf+1)/2) * W/nf * 0.29' as='int((nf+2)/2) * W/nf * 0.29'
+ pd='2*int((nf+1)/2) * (W/nf + 0.29)' ps='2*int((nf+2)/2) * (W/nf + 0.29)' nrd='0.29 / W' nrs='0.29 / W'
+ sa=0 sb=0 sd=0 mult=1 m=1
XM58 VN VN VCP VN sky130_fd_pr__nfet_01v8 L=0.5 W=12 nf=1 ad='int((nf+1)/2) * W/nf * 0.29' as='int((nf+2)/2) * W/nf * 0.29'
+ pd='2*int((nf+1)/2) * (W/nf + 0.29)' ps='2*int((nf+2)/2) * (W/nf + 0.29)' nrd='0.29 / W' nrs='0.29 / W'
+ sa=0 sb=0 sd=0 mult=1 m=1
XM59 VCP VN VN VN sky130_fd_pr__nfet_01v8 L=0.5 W=12 nf=1 ad='int((nf+1)/2) * W/nf * 0.29' as='int((nf+2)/2) * W/nf * 0.29'
+ pd='2*int((nf+1)/2) * (W/nf + 0.29)' ps='2*int((nf+2)/2) * (W/nf + 0.29)' nrd='0.29 / W' nrs='0.29 / W'
+ sa=0 sb=0 sd=0 mult=1 m=1
XM3b VP VBP VBP VDD sky130_fd_pr__pfet_01v8 L=0.5 W=3 nf=1 ad='int((nf+1)/2) * W/nf * 0.29' as='int((nf+2)/2) * W/nf * 0.29'
+ pd='2*int((nf+1)/2) * (W/nf + 0.29)' ps='2*int((nf+2)/2) * (W/nf + 0.29)' nrd='0.29 / W' nrs='0.29 / W'
+ sa=0 sb=0 sd=0 mult=1 m=1
XM3a VBN VBP VP VDD sky130_fd_pr__pfet_01v8 L=0.5 W=3 nf=1 ad='int((nf+1)/2) * W/nf * 0.29' as='int((nf+2)/2) * W/nf * 0.29'
+ pd='2*int((nf+1)/2) * (W/nf + 0.29)' ps='2*int((nf+2)/2) * (W/nf + 0.29)' nrd='0.29 / W' nrs='0.29 / W'
+ sa=0 sb=0 sd=0 mult=1 m=1
XM4a VBP VBP VP VDD sky130_fd_pr__pfet_01v8 L=0.5 W=3 nf=1 ad='int((nf+1)/2) * W/nf * 0.29' as='int((nf+2)/2) * W/nf * 0.29'
+ pd='2*int((nf+1)/2) * (W/nf + 0.29)' ps='2*int((nf+2)/2) * (W/nf + 0.29)' nrd='0.29 / W' nrs='0.29 / W'
+ sa=0 sb=0 sd=0 mult=1 m=1
XM4b VP VBP VBN VDD sky130_fd_pr__pfet_01v8 L=0.5 W=3 nf=1 ad='int((nf+1)/2) * W/nf * 0.29' as='int((nf+2)/2) * W/nf * 0.29'
+ pd='2*int((nf+1)/2) * (W/nf + 0.29)' ps='2*int((nf+2)/2) * (W/nf + 0.29)' nrd='0.29 / W' nrs='0.29 / W'
+ sa=0 sb=0 sd=0 mult=1 m=1
XM3c VBN VBP VP VDD sky130_fd_pr__pfet_01v8 L=0.5 W=3 nf=1 ad='int((nf+1)/2) * W/nf * 0.29' as='int((nf+2)/2) * W/nf * 0.29'
+ pd='2*int((nf+1)/2) * (W/nf + 0.29)' ps='2*int((nf+2)/2) * (W/nf + 0.29)' nrd='0.29 / W' nrs='0.29 / W'
+ sa=0 sb=0 sd=0 mult=1 m=1
XM3d VP VBP VBP VDD sky130_fd_pr__pfet_01v8 L=0.5 W=3 nf=1 ad='int((nf+1)/2) * W/nf * 0.29' as='int((nf+2)/2) * W/nf * 0.29'
+ pd='2*int((nf+1)/2) * (W/nf + 0.29)' ps='2*int((nf+2)/2) * (W/nf + 0.29)' nrd='0.29 / W' nrs='0.29 / W'
+ sa=0 sb=0 sd=0 mult=1 m=1
XM4c VBP VBP VP VDD sky130_fd_pr__pfet_01v8 L=0.5 W=3 nf=1 ad='int((nf+1)/2) * W/nf * 0.29' as='int((nf+2)/2) * W/nf * 0.29'
+ pd='2*int((nf+1)/2) * (W/nf + 0.29)' ps='2*int((nf+2)/2) * (W/nf + 0.29)' nrd='0.29 / W' nrs='0.29 / W'
+ sa=0 sb=0 sd=0 mult=1 m=1
XM1e VP VP VBN VP sky130_fd_pr__pfet_01v8 L=0.5 W=3 nf=1 ad='int((nf+1)/2) * W/nf * 0.29' as='int((nf+2)/2) * W/nf * 0.29'
+ pd='2*int((nf+1)/2) * (W/nf + 0.29)' ps='2*int((nf+2)/2) * (W/nf + 0.29)' nrd='0.29 / W' nrs='0.29 / W'
+ sa=0 sb=0 sd=0 mult=1 m=1
XM1f VBN VP VP VP sky130_fd_pr__pfet_01v8 L=0.5 W=3 nf=1 ad='int((nf+1)/2) * W/nf * 0.29' as='int((nf+2)/2) * W/nf * 0.29'
+ pd='2*int((nf+1)/2) * (W/nf + 0.29)' ps='2*int((nf+2)/2) * (W/nf + 0.29)' nrd='0.29 / W' nrs='0.29 / W'
+ sa=0 sb=0 sd=0 mult=1 m=1
XM4d VP VBP VBN VDD sky130_fd_pr__pfet_01v8 L=0.5 W=3 nf=1 ad='int((nf+1)/2) * W/nf * 0.29' as='int((nf+2)/2) * W/nf * 0.29'
+ pd='2*int((nf+1)/2) * (W/nf + 0.29)' ps='2*int((nf+2)/2) * (W/nf + 0.29)' nrd='0.29 / W' nrs='0.29 / W'
+ sa=0 sb=0 sd=0 mult=1 m=1
XM60 VBN VBN VN GND sky130_fd_pr__nfet_01v8 L=0.5 W=12 nf=1 ad='int((nf+1)/2) * W/nf * 0.29' as='int((nf+2)/2) * W/nf * 0.29'
+ pd='2*int((nf+1)/2) * (W/nf + 0.29)' ps='2*int((nf+2)/2) * (W/nf + 0.29)' nrd='0.29 / W' nrs='0.29 / W'
+ sa=0 sb=0 sd=0 mult=1 m=1
.ends

.GLOBAL GND
.GLOBAL VDD
.end
